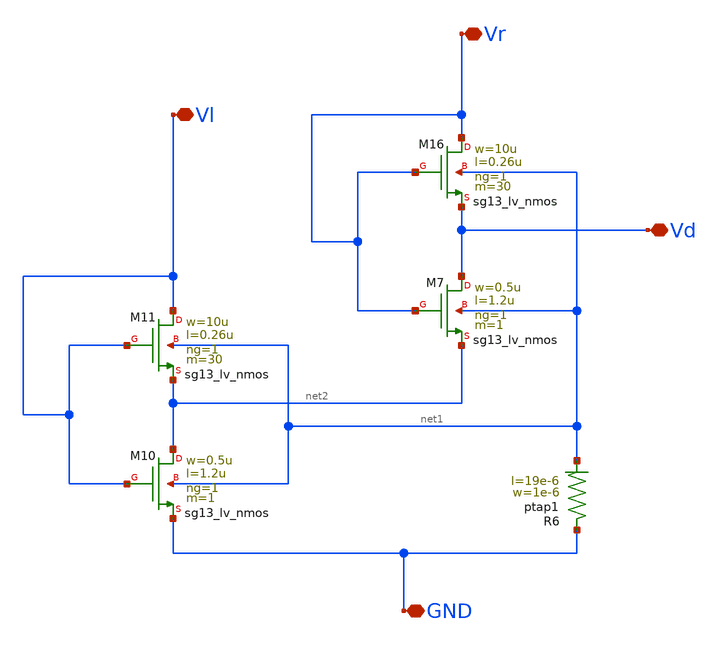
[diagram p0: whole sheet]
** sch_path: Layouts/ib_ctat_ptat/SCCT_PTAT.sch
**.subckt SCCT_PTAT GND Vd Vr Vl
*.iopin GND
*.iopin Vd
*.iopin Vr
*.iopin Vl
XM7 Vd Vr net2 net1 sg13_lv_nmos w=0.5u l=1.2u ng=1 m=1 mm_ok=1
XM10 net2 Vl GND net1 sg13_lv_nmos w=0.5u l=1.2u ng=1 m=1 mm_ok=1
XM11 Vl Vl net2 net1 sg13_lv_nmos w=10u l=0.26u ng=1 m=30 mm_ok=1
XM16 Vr Vr Vd net1 sg13_lv_nmos w=10u l=0.26u ng=1 m=30 mm_ok=1
XR6 GND net1 ptap1 R=16.61 w=1e-6 l=19e-6
**.ends
.end
